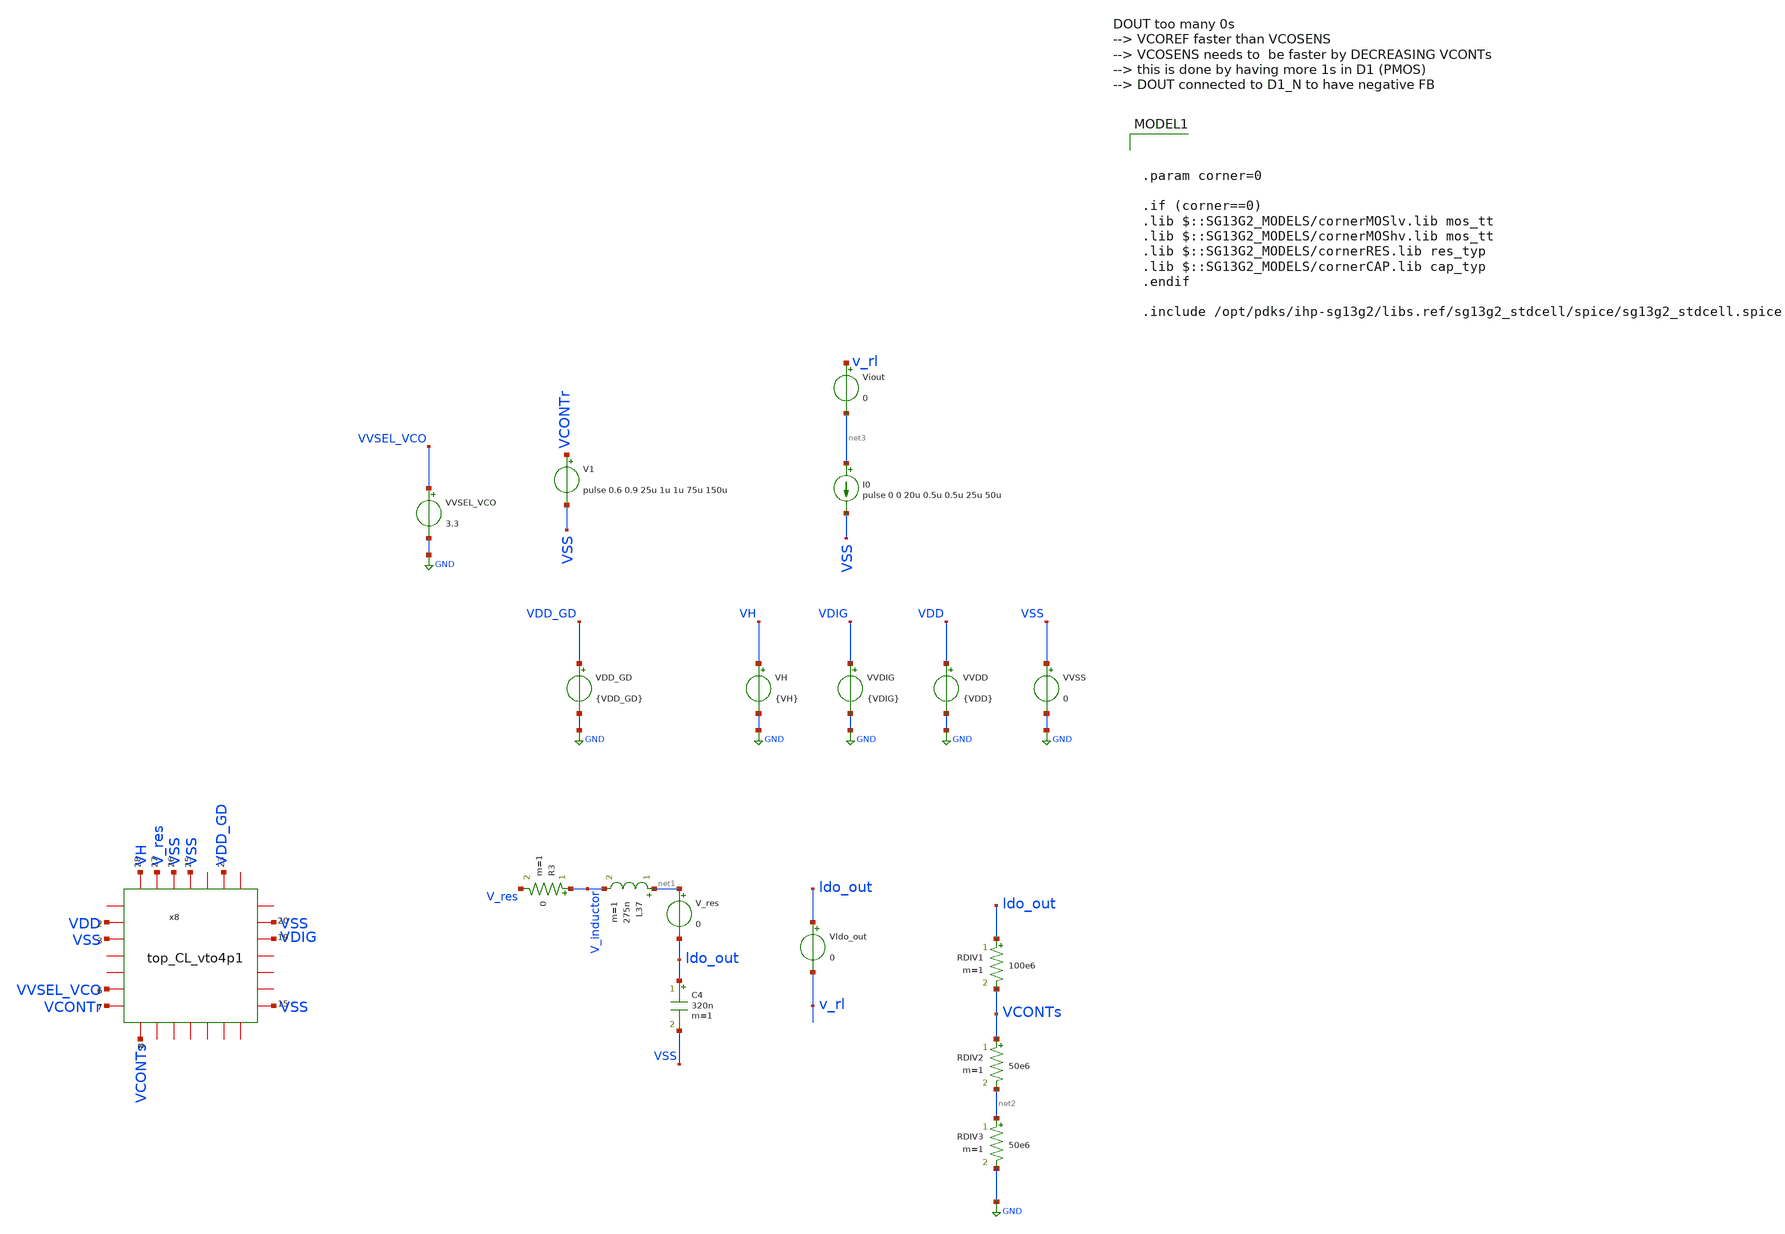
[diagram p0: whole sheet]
** sch_path: ChipUSM_AnalogTrack24/top/tb_TDBuckTOP_vto4p2.sch
**.subckt tb_TDBuckTOP_vto4p2
L37 net1 V_inductor 275n m=1
R3 V_inductor V_res 0 m=1
V_res net1 ldo_out 0
VH VH GND {VH}
VVDIG VDIG GND {VDIG}
C4 ldo_out VSS 320n m=1
Vldo_out ldo_out v_rl 0
RDIV1 ldo_out VCONTs 100e6 m=1
RDIV2 VCONTs net2 50e6 m=1
RDIV3 net2 GND 50e6 m=1
VDD_GD VDD_GD GND {VDD_GD}
V1 VCONTr VSS pulse 0.6 0.9 25u 1u 1u 75u 150u
x8 VH VDD_GD VSS V_res VSS VDD VSS VSS VDIG VSS VCONTr VCONTs VVSEL_VCO top_CL_vto4p1
VVDD VDD GND {VDD}
VVSS VSS GND 0
I0 net3 VSS pulse 0 0 20u 0.5u 0.5u 25u 50u
Viout v_rl net3 0
VVSEL_VCO VVSEL_VCO GND 3.3
**** begin user architecture code

.param VDIG = 1.2
.param VH = 3.3
.param VDD = 3.3
.param VDD_GD = 3.3
*LATEST TDBuckLOADS
*1000mA
*RL v_rl gnd R = 'TIME > 25u ? 120:1.2'
RL v_rl gnd 2.4
*100mA
*.param RL = 12
*80mA
*.param RL = 15
*40mA
*.param RL = 30
*20mA
*.param RL = 60
*10mA
*.param RL = 120
.save v(ldo_out) v(v_res) v(x8.D1) v(x8.D1_N) v(x8.x17.16) v(VCONTr) v(VCONTs) v(x8.V_1r) v(x8.V_1s) v(x8.V_1r_dl) v(x8.V_1s_dl) v(x8.V_1r_buff) v(x8.V_1s_buff) v(x8.V_1r_buff_sp) v(x8.V_1s_buff_sp) v(vh) i(vh) v(vdd_gd) i(vdd_gd) i(v_res) v(x8.vcp) v(x8.vcn) i(vldo_out) i(vvdig) i(vvdd) i(Viout)
*vvdd vdd 0 dc 3.3
*vvss vss 0 0
*vvcontr VCONTr 0 dc 0.6
*vvconts VCONTs 0 dc 0.61
*.option temp = 200
.ic v(VCONTs) = 0.6
.ic v(x8.V_1s) = 0
.ic v(x8.x5.V_2s) = 3.3
.ic v(x8.V_1r) = 3.3
.ic v(x8.x2.V_2r) = 0
.ic v(ldo_out) = 1.2
*.ic v(V_res) = 1.2
.ic v(V_inductor) = 1.2

.option method=gear
.option cshunt=0.01e-12

.control
*tran 2n 1m
*tran 4n 250u
tran 100p 150u
*wrdata
*+ /home/designer/shared/TORepo_IHPNov2024_TDBuck/design_data/xschem/sim_data/data_TDBuckTOP_vto4p1.txt tran.v(ldo_out) tran.i(vldo_out) tran.i(vh) tran.i(vdd_gd) tran.i(vvdig) tran.i(vvdd)
plot v(ldo_out)
plot v(v_res)
plot v(x8.D1) v(x8.D1_N) i(VH)
plot v(x8.x17.16)
plot v(VCONTr) v(VCONTs)
plot v(x8.V_1r_buff) v(x8.V_1s_buff)+2 v(x8.x17.16)+4
plot i(vldo_out)
*plot v(VCONTs_OL)
.endc




.param corner=0

.if (corner==0)
.lib $::SG13G2_MODELS/cornerMOSlv.lib mos_tt
.lib $::SG13G2_MODELS/cornerMOShv.lib mos_tt
.lib $::SG13G2_MODELS/cornerRES.lib res_typ
.lib $::SG13G2_MODELS/cornerCAP.lib cap_typ
.endif

.include /opt/pdks/ihp-sg13g2/libs.ref/sg13g2_stdcell/spice/sg13g2_stdcell.spice

**** end user architecture code
**.ends
.GLOBAL GND
.end
